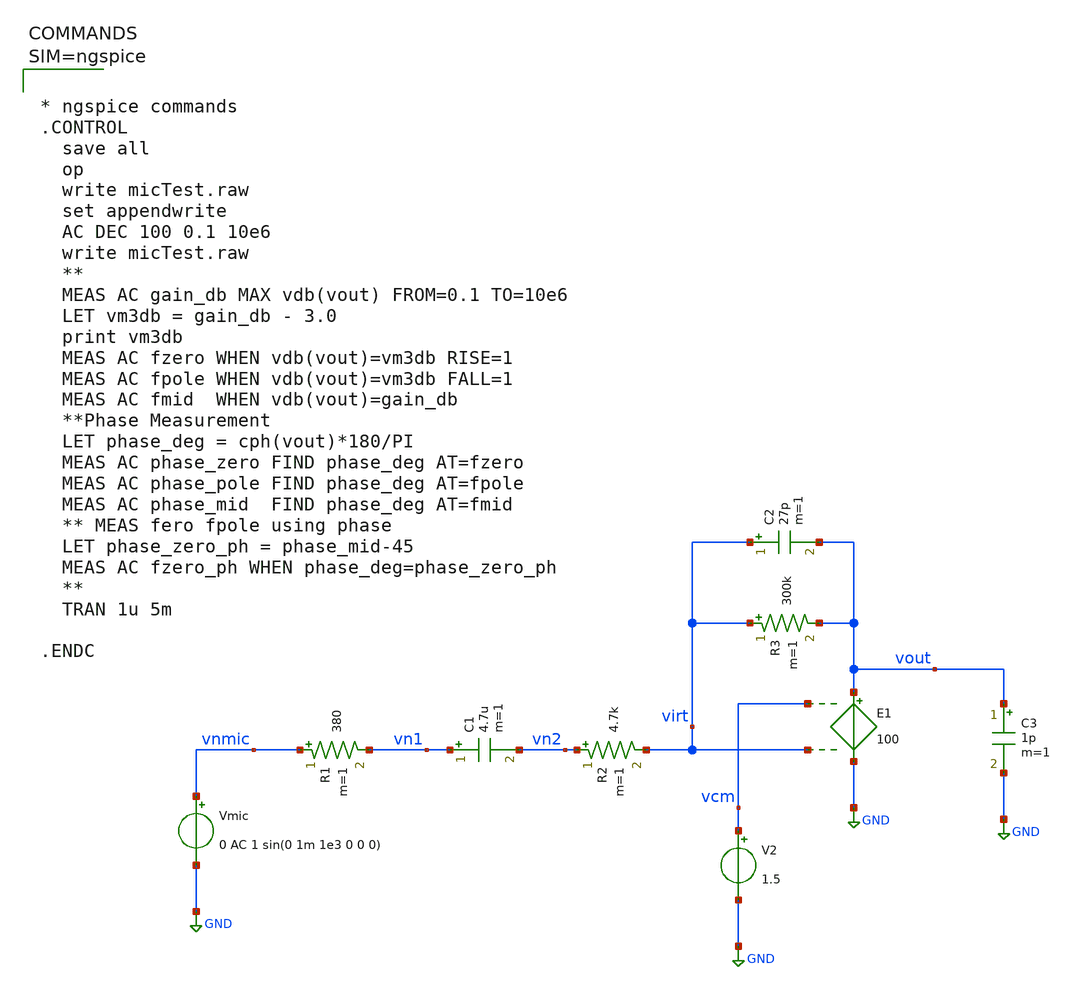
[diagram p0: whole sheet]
** sch_path: xschem/micTest.sch
**.subckt micTest
Vmic vnmic GND 0 AC 1 sin(0 1m 1e3 0 0 0)
R1 vnmic vn1 380 m=1
C1 vn1 vn2 4.7u m=1
R2 vn2 virt 4.7k m=1
E1 vout GND vcm virt 100
R3 virt vout 300k m=1
C2 virt vout 27p m=1
V2 vcm GND 1.5
C3 vout GND 1p m=1
**** begin user architecture code



* ngspice commands
.CONTROL
  save all
  op
  write micTest.raw
  set appendwrite
  AC DEC 100 0.1 10e6
  write micTest.raw
  **
  MEAS AC gain_db MAX vdb(vout) FROM=0.1 TO=10e6
  LET vm3db = gain_db - 3.0
  print vm3db
  MEAS AC fzero WHEN vdb(vout)=vm3db RISE=1
  MEAS AC fpole WHEN vdb(vout)=vm3db FALL=1
  MEAS AC fmid  WHEN vdb(vout)=gain_db
  **Phase Measurement
  LET phase_deg = cph(vout)*180/PI
  MEAS AC phase_zero FIND phase_deg AT=fzero
  MEAS AC phase_pole FIND phase_deg AT=fpole
  MEAS AC phase_mid  FIND phase_deg AT=fmid
  ** MEAS fero fpole using phase
  LET phase_zero_ph = phase_mid-45
  MEAS AC fzero_ph WHEN phase_deg=phase_zero_ph
  **
  TRAN 1u 5m

.ENDC



**** end user architecture code
**.ends
.GLOBAL GND
.end
